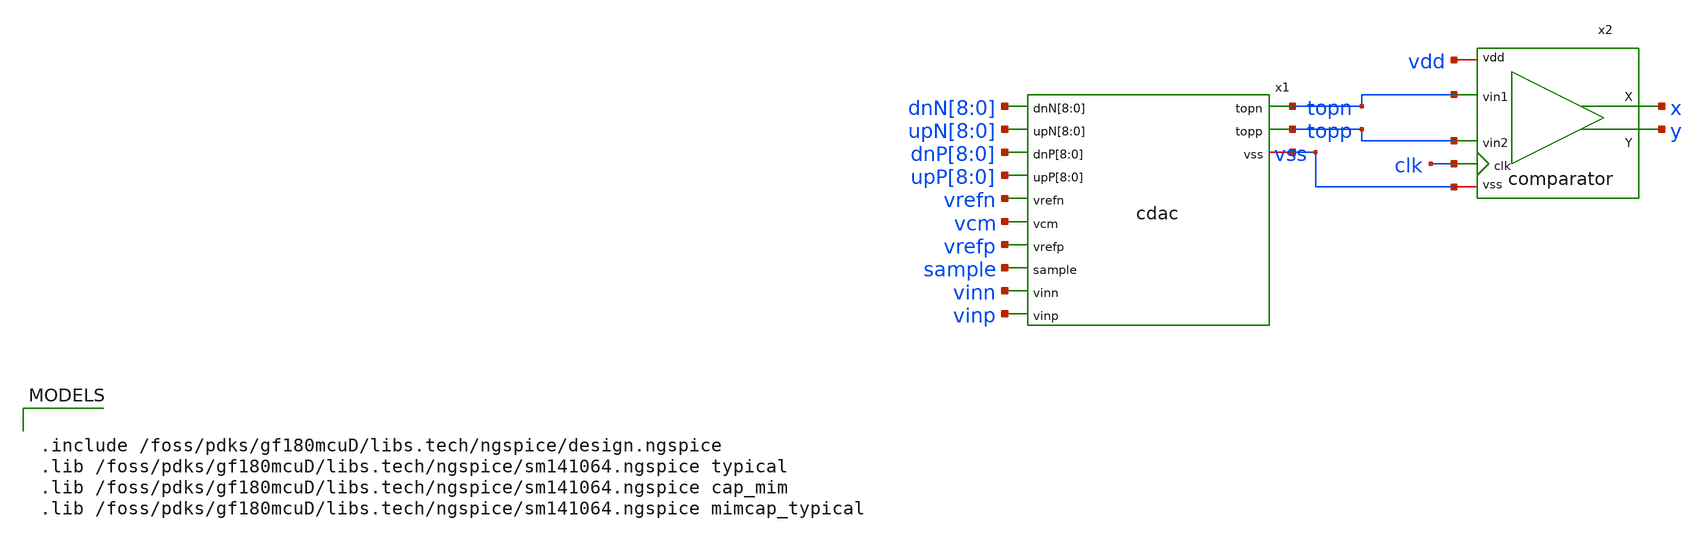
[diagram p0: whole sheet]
** sch_path: designs/libs/core_analog/saradc/tb/sar_cl_tb.sch
**.subckt sar_cl_tb
x1 dnN[8] dnN[7] dnN[6] dnN[5] dnN[4] dnN[3] dnN[2] dnN[1] dnN[0] upN[8] upN[7] upN[6] upN[5] upN[4]
+ upN[3] upN[2] upN[1] upN[0] dnP[8] dnP[7] dnP[6] dnP[5] dnP[4] dnP[3] dnP[2] dnP[1] dnP[0] upP[8] upP[7]
+ upP[6] upP[5] upP[4] upP[3] upP[2] upP[1] upP[0] topn topp vss vrefn vcm vrefp sample vinn vinp cdac
x2 vdd vss x topn y topp clk comparator
**** begin user architecture code


.include /foss/pdks/gf180mcuD/libs.tech/ngspice/design.ngspice
.lib /foss/pdks/gf180mcuD/libs.tech/ngspice/sm141064.ngspice typical
.lib /foss/pdks/gf180mcuD/libs.tech/ngspice/sm141064.ngspice cap_mim
.lib /foss/pdks/gf180mcuD/libs.tech/ngspice/sm141064.ngspice mimcap_typical




* ============ SAR closed-loop reactive TB ============
* SAR FSM lives in .control: sample -> 10x[ stop@eval, read v(x),
* decide bit (X>1.65 => 1), alter CDAC caps per SAR rule, resume ].
* Drive .param vid from the notebook (vid = (code-512)*LSB + LSB/2) for
* code reproduction and coherent-sine ENOB sweeps.
* SAR rule: bit=1 -> dnP[c]+upN[c] ; bit=0 -> upP[c]+dnN[c] ; cap c=k-1, MSB free.

* ---- supplies / refs / clock / loads ----
Vvdd vdd 0 3.3
Vvss vss 0 0
Vvrefp vrefp 0 1
Vvrefn vrefn 0 0
Vvcm vcm 0 0.5
Vsample sample 0 PWL(0 3.3 9n 3.3 9.05n 0)
Vclk clk 0 pulse(0 3.3 15n 50p 50p 4n 10n)
Cx x 0 20f
Cy y 0 20f

* ---- differential input (override vid externally) ----
.param CM = 1.65
.param vid = 0.9385
Vvinp vinp 0 'CM+vid/2'
Vvinn vinn 0 'CM-vid/2'

* ---- 36 CDAC control sources (idle; reactively altered) ----
VupP8 upP[8] 0 0
VupP7 upP[7] 0 0
VupP6 upP[6] 0 0
VupP5 upP[5] 0 0
VupP4 upP[4] 0 0
VupP3 upP[3] 0 0
VupP2 upP[2] 0 0
VupP1 upP[1] 0 0
VupP0 upP[0] 0 0
VdnP8 dnP[8] 0 0
VdnP7 dnP[7] 0 0
VdnP6 dnP[6] 0 0
VdnP5 dnP[5] 0 0
VdnP4 dnP[4] 0 0
VdnP3 dnP[3] 0 0
VdnP2 dnP[2] 0 0
VdnP1 dnP[1] 0 0
VdnP0 dnP[0] 0 0
VupN8 upN[8] 0 0
VupN7 upN[7] 0 0
VupN6 upN[6] 0 0
VupN5 upN[5] 0 0
VupN4 upN[4] 0 0
VupN3 upN[3] 0 0
VupN2 upN[2] 0 0
VupN1 upN[1] 0 0
VupN0 upN[0] 0 0
VdnN8 dnN[8] 0 0
VdnN7 dnN[7] 0 0
VdnN6 dnN[6] 0 0
VdnN5 dnN[5] 0 0
VdnN4 dnN[4] 0 0
VdnN3 dnN[3] 0 0
VdnN2 dnN[2] 0 0
VdnN1 dnN[1] 0 0
VdnN0 dnN[0] 0 0

* ---- transient (stepped by control breakpoints) ----
.tran 20p 112n uic

.control
set noaskquit
save x topp topn
stop when time = 18.6n
stop when time = 28.6n
stop when time = 38.6n
stop when time = 48.6n
stop when time = 58.6n
stop when time = 68.6n
stop when time = 78.6n
stop when time = 88.6n
stop when time = 98.6n
stop when time = 108.6n
run
let nlast = length(v(x)) - 1
let xlast = v(x)[nlast]
if (xlast > 1.65)
  let b9 = 1
  alter VdnP8 = 3.3
  alter VupN8 = 3.3
else
  let b9 = 0
  alter VupP8 = 3.3
  alter VdnN8 = 3.3
end
resume
let nlast = length(v(x)) - 1
let xlast = v(x)[nlast]
if (xlast > 1.65)
  let b8 = 1
  alter VdnP7 = 3.3
  alter VupN7 = 3.3
else
  let b8 = 0
  alter VupP7 = 3.3
  alter VdnN7 = 3.3
end
resume
let nlast = length(v(x)) - 1
let xlast = v(x)[nlast]
if (xlast > 1.65)
  let b7 = 1
  alter VdnP6 = 3.3
  alter VupN6 = 3.3
else
  let b7 = 0
  alter VupP6 = 3.3
  alter VdnN6 = 3.3
end
resume
let nlast = length(v(x)) - 1
let xlast = v(x)[nlast]
if (xlast > 1.65)
  let b6 = 1
  alter VdnP5 = 3.3
  alter VupN5 = 3.3
else
  let b6 = 0
  alter VupP5 = 3.3
  alter VdnN5 = 3.3
end
resume
let nlast = length(v(x)) - 1
let xlast = v(x)[nlast]
if (xlast > 1.65)
  let b5 = 1
  alter VdnP4 = 3.3
  alter VupN4 = 3.3
else
  let b5 = 0
  alter VupP4 = 3.3
  alter VdnN4 = 3.3
end
resume
let nlast = length(v(x)) - 1
let xlast = v(x)[nlast]
if (xlast > 1.65)
  let b4 = 1
  alter VdnP3 = 3.3
  alter VupN3 = 3.3
else
  let b4 = 0
  alter VupP3 = 3.3
  alter VdnN3 = 3.3
end
resume
let nlast = length(v(x)) - 1
let xlast = v(x)[nlast]
if (xlast > 1.65)
  let b3 = 1
  alter VdnP2 = 3.3
  alter VupN2 = 3.3
else
  let b3 = 0
  alter VupP2 = 3.3
  alter VdnN2 = 3.3
end
resume
let nlast = length(v(x)) - 1
let xlast = v(x)[nlast]
if (xlast > 1.65)
  let b2 = 1
  alter VdnP1 = 3.3
  alter VupN1 = 3.3
else
  let b2 = 0
  alter VupP1 = 3.3
  alter VdnN1 = 3.3
end
resume
let nlast = length(v(x)) - 1
let xlast = v(x)[nlast]
if (xlast > 1.65)
  let b1 = 1
  alter VdnP0 = 3.3
  alter VupN0 = 3.3
else
  let b1 = 0
  alter VupP0 = 3.3
  alter VdnN0 = 3.3
end
resume
let nlast = length(v(x)) - 1
let xlast = v(x)[nlast]
if (xlast > 1.65)
  let b0 = 1
else
  let b0 = 0
end
let code = b9*512 + b8*256 + b7*128 + b6*64 + b5*32 + b4*16 + b3*8 + b2*4 + b1*2 + b0*1
echo RESULT_CODE_BELOW
print code
.endc


**** end user architecture code
**.ends
.end
